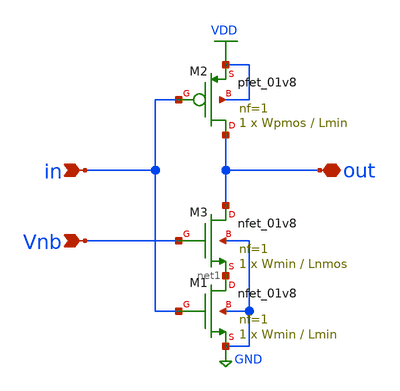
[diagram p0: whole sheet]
** sch_path: xschem/inv/inv_weak_pulldown.sch
**.subckt inv_weak_pulldown in out Vnb
*.ipin in
*.iopin out
*.ipin Vnb
XM1 net1 in GND GND sky130_fd_pr__nfet_01v8 L=Lmin W=Wmin nf=1 ad='int((nf+1)/2) * W/nf * 0.29' as='int((nf+2)/2) * W/nf * 0.29'
+ pd='2*int((nf+1)/2) * (W/nf + 0.29)' ps='2*int((nf+2)/2) * (W/nf + 0.29)' nrd='0.29 / W' nrs='0.29 / W'
+ sa=0 sb=0 sd=0 mult=1 m=1
XM2 out in VDD VDD sky130_fd_pr__pfet_01v8 L=Lmin W=Wpmos nf=1 ad='int((nf+1)/2) * W/nf * 0.29' as='int((nf+2)/2) * W/nf * 0.29'
+ pd='2*int((nf+1)/2) * (W/nf + 0.29)' ps='2*int((nf+2)/2) * (W/nf + 0.29)' nrd='0.29 / W' nrs='0.29 / W'
+ sa=0 sb=0 sd=0 mult=1 m=1
XM3 out Vnb net1 GND sky130_fd_pr__nfet_01v8 L=Lnmos W=Wmin nf=1 ad='int((nf+1)/2) * W/nf * 0.29' as='int((nf+2)/2) * W/nf * 0.29'
+ pd='2*int((nf+1)/2) * (W/nf + 0.29)' ps='2*int((nf+2)/2) * (W/nf + 0.29)' nrd='0.29 / W' nrs='0.29 / W'
+ sa=0 sb=0 sd=0 mult=1 m=1
**.ends
.GLOBAL VDD
.GLOBAL GND
.end
